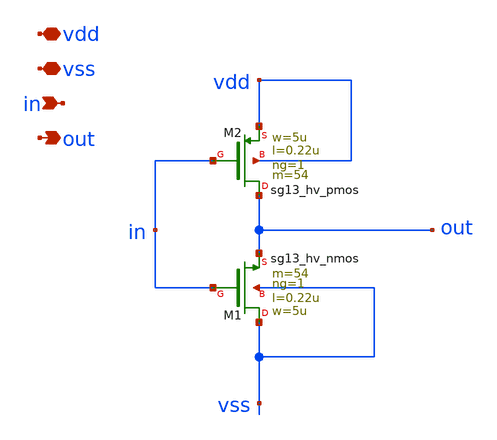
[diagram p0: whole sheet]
** sch_path: ChipUSM_AnalogTrack24/inv/inv.sch
**.subckt inv vdd vss in out
*.iopin vdd
*.iopin vss
*.ipin in
*.opin out
XM1 vss in out vss sg13_hv_nmos w=5u l=0.22u ng=1 m=54 mm_ok=1
XM2 out in vdd vdd sg13_hv_pmos w=5u l=0.22u ng=1 m=54 mm_ok=1
**.ends
.end
